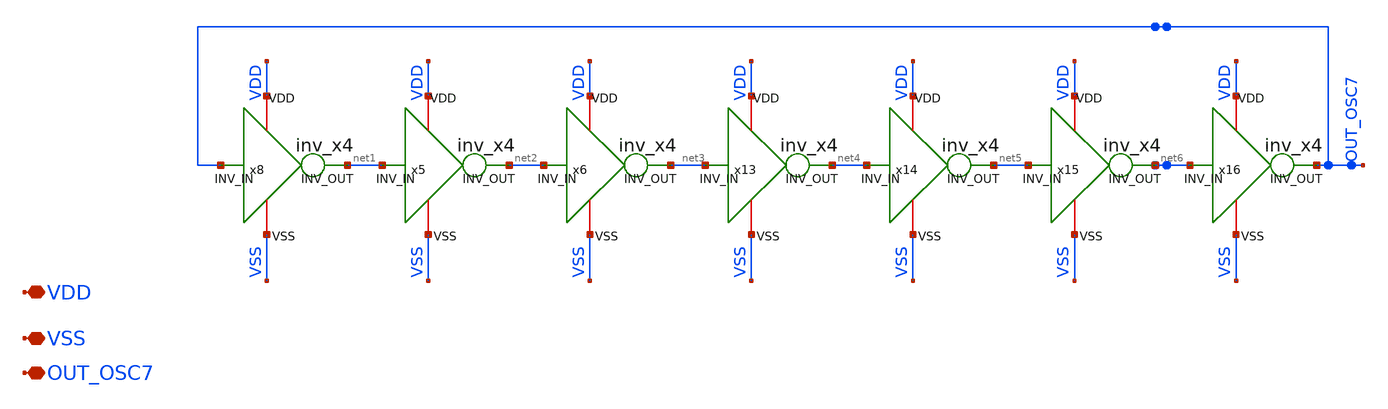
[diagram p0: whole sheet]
** sch_path: xschem/OSC7.sch
**.subckt OSC7 VDD VSS OUT_OSC7
*.iopin VDD
*.iopin VSS
*.iopin OUT_OSC7
x8 VDD VSS net1 OUT_OSC7 inv_x4
x5 VDD VSS net2 net1 inv_x4
x6 VDD VSS net3 net2 inv_x4
x13 VDD VSS net4 net3 inv_x4
x14 VDD VSS net5 net4 inv_x4
x15 VDD VSS net6 net5 inv_x4
x16 VDD VSS OUT_OSC7 net6 inv_x4
**.ends

* expanding   symbol:  inv_x4.sym # of pins=4
** sym_path: xschem/inv_x4.sym
** sch_path: xschem/inv_x4.sch
.subckt inv_x4 VDD VSS INV_OUT INV_IN
*.ipin INV_IN
*.opin INV_OUT
*.iopin VDD
*.iopin VSS
XM3 INV_OUT INV_IN VDD VDD sky130_fd_pr__pfet_01v8 L=10 W=2 nf=1 ad='int((nf+1)/2) * W/nf * 0.29' as='int((nf+2)/2) * W/nf * 0.29'
+ pd='2*int((nf+1)/2) * (W/nf + 0.29)' ps='2*int((nf+2)/2) * (W/nf + 0.29)' nrd='0.29 / W' nrs='0.29 / W'
+ sa=0 sb=0 sd=0 mult=1 m=1
XM5 INV_OUT INV_IN VSS VSS sky130_fd_pr__nfet_01v8 L=10 W=1 nf=1 ad='int((nf+1)/2) * W/nf * 0.29' as='int((nf+2)/2) * W/nf * 0.29'
+ pd='2*int((nf+1)/2) * (W/nf + 0.29)' ps='2*int((nf+2)/2) * (W/nf + 0.29)' nrd='0.29 / W' nrs='0.29 / W'
+ sa=0 sb=0 sd=0 mult=1 m=1
.ends

.end
